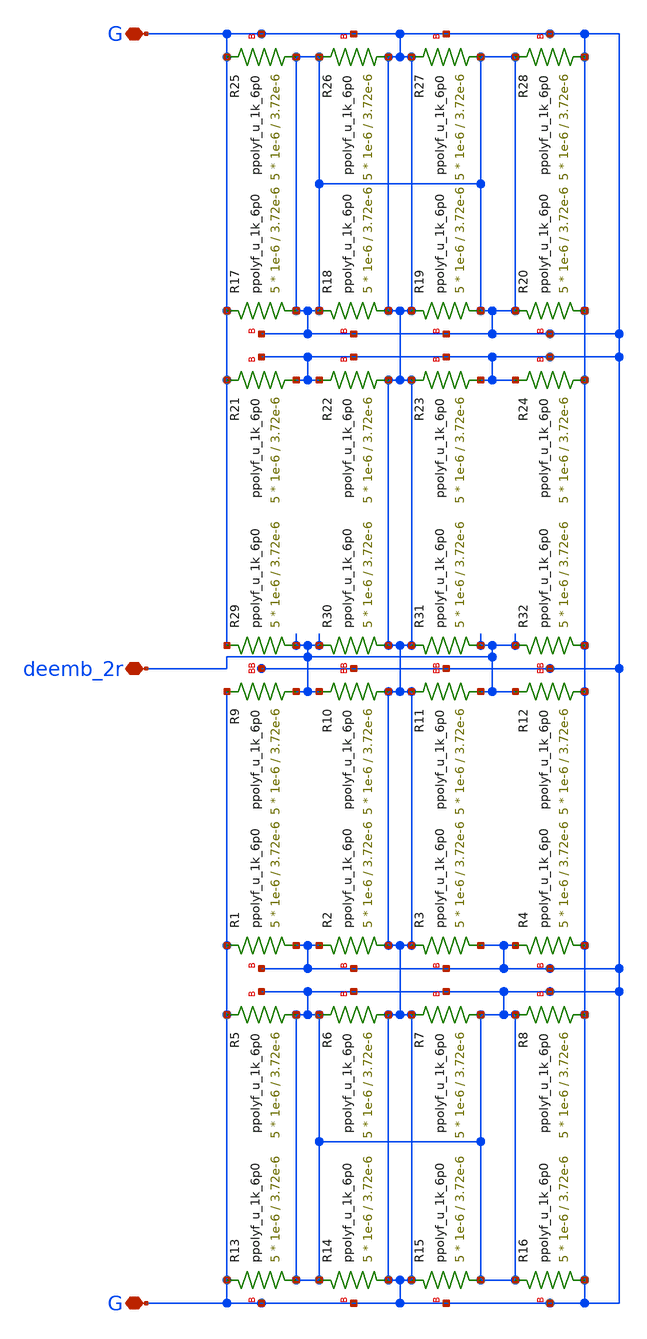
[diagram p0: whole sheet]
** sch_path: xschem/DEEMB_2R.sch
**.subckt DEEMB_2R G deemb_2r G
*.iopin G
*.iopin deemb_2r
*.iopin G
XR1 G G G ppolyf_u_1k_6p0 r_width=1e-6 r_length=3.72e-6 m=5
XR2 G G G ppolyf_u_1k_6p0 r_width=1e-6 r_length=3.72e-6 m=5
XR3 G G G ppolyf_u_1k_6p0 r_width=1e-6 r_length=3.72e-6 m=5
XR4 G G G ppolyf_u_1k_6p0 r_width=1e-6 r_length=3.72e-6 m=5
XR5 G G G ppolyf_u_1k_6p0 r_width=1e-6 r_length=3.72e-6 m=5
XR6 G G G ppolyf_u_1k_6p0 r_width=1e-6 r_length=3.72e-6 m=5
XR7 G G G ppolyf_u_1k_6p0 r_width=1e-6 r_length=3.72e-6 m=5
XR8 G G G ppolyf_u_1k_6p0 r_width=1e-6 r_length=3.72e-6 m=5
XR9 deemb_2r G G ppolyf_u_1k_6p0 r_width=1e-6 r_length=3.72e-6 m=5
XR10 G deemb_2r G ppolyf_u_1k_6p0 r_width=1e-6 r_length=3.72e-6 m=5
XR11 deemb_2r G G ppolyf_u_1k_6p0 r_width=1e-6 r_length=3.72e-6 m=5
XR12 G deemb_2r G ppolyf_u_1k_6p0 r_width=1e-6 r_length=3.72e-6 m=5
XR13 G G G ppolyf_u_1k_6p0 r_width=1e-6 r_length=3.72e-6 m=5
XR14 G G G ppolyf_u_1k_6p0 r_width=1e-6 r_length=3.72e-6 m=5
XR15 G G G ppolyf_u_1k_6p0 r_width=1e-6 r_length=3.72e-6 m=5
XR16 G G G ppolyf_u_1k_6p0 r_width=1e-6 r_length=3.72e-6 m=5
XR17 G G G ppolyf_u_1k_6p0 r_width=1e-6 r_length=3.72e-6 m=5
XR18 G G G ppolyf_u_1k_6p0 r_width=1e-6 r_length=3.72e-6 m=5
XR19 G G G ppolyf_u_1k_6p0 r_width=1e-6 r_length=3.72e-6 m=5
XR20 G G G ppolyf_u_1k_6p0 r_width=1e-6 r_length=3.72e-6 m=5
XR21 G G G ppolyf_u_1k_6p0 r_width=1e-6 r_length=3.72e-6 m=5
XR22 G G G ppolyf_u_1k_6p0 r_width=1e-6 r_length=3.72e-6 m=5
XR23 G G G ppolyf_u_1k_6p0 r_width=1e-6 r_length=3.72e-6 m=5
XR24 G G G ppolyf_u_1k_6p0 r_width=1e-6 r_length=3.72e-6 m=5
XR25 G G G ppolyf_u_1k_6p0 r_width=1e-6 r_length=3.72e-6 m=5
XR26 G G G ppolyf_u_1k_6p0 r_width=1e-6 r_length=3.72e-6 m=5
XR27 G G G ppolyf_u_1k_6p0 r_width=1e-6 r_length=3.72e-6 m=5
XR28 G G G ppolyf_u_1k_6p0 r_width=1e-6 r_length=3.72e-6 m=5
XR29 deemb_2r G G ppolyf_u_1k_6p0 r_width=1e-6 r_length=3.72e-6 m=5
XR30 G deemb_2r G ppolyf_u_1k_6p0 r_width=1e-6 r_length=3.72e-6 m=5
XR31 deemb_2r G G ppolyf_u_1k_6p0 r_width=1e-6 r_length=3.72e-6 m=5
XR32 G deemb_2r G ppolyf_u_1k_6p0 r_width=1e-6 r_length=3.72e-6 m=5
**.ends
.end
